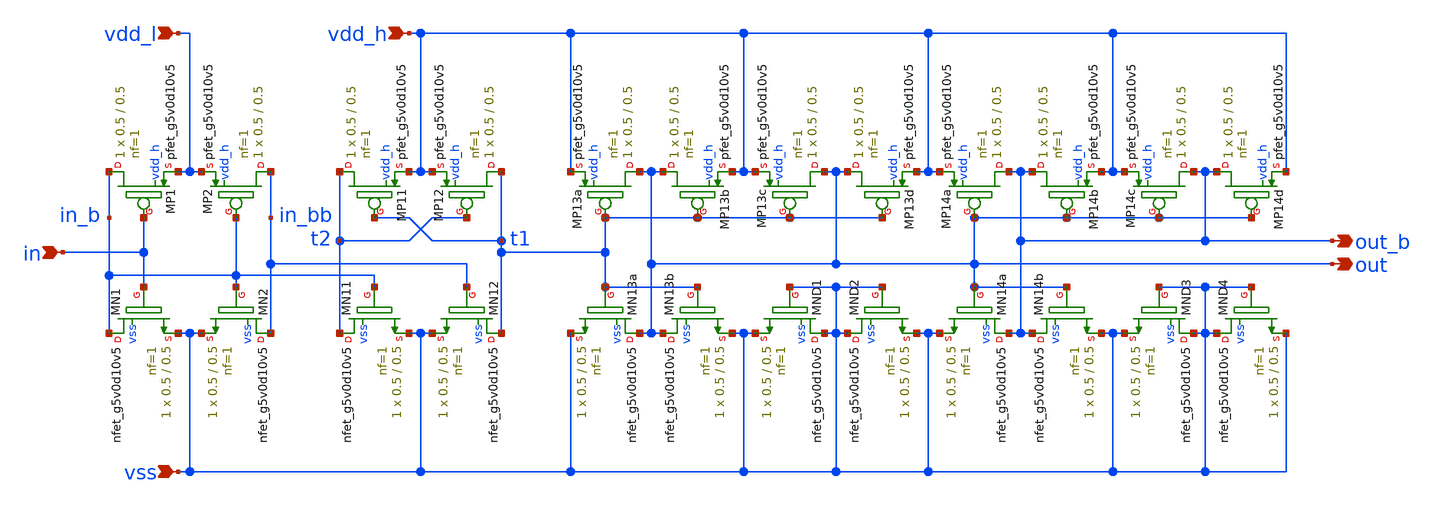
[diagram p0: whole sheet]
** sch_path: xschem/lsi1v8o5v0.sch
**.subckt lsi1v8o5v0 in out_b out vdd_l vdd_h vss
*.ipin in
*.opin out_b
*.opin out
*.ipin vdd_l
*.ipin vdd_h
*.ipin vss
XMN2 in_bb in_b vss vss sky130_fd_pr__nfet_g5v0d10v5 L=0.5 W=0.5 nf=1 ad='int((nf+1)/2) * W/nf * 0.29'
+ as='int((nf+2)/2) * W/nf * 0.29' pd='2*int((nf+1)/2) * (W/nf + 0.29)' ps='2*int((nf+2)/2) * (W/nf + 0.29)'
+ nrd='0.29 / W' nrs='0.29 / W' sa=0 sb=0 sd=0 mult=1 m=1
XMN11 t2 in_b vss vss sky130_fd_pr__nfet_g5v0d10v5 L=0.5 W=0.5 nf=1 ad='int((nf+1)/2) * W/nf * 0.29'
+ as='int((nf+2)/2) * W/nf * 0.29' pd='2*int((nf+1)/2) * (W/nf + 0.29)' ps='2*int((nf+2)/2) * (W/nf + 0.29)'
+ nrd='0.29 / W' nrs='0.29 / W' sa=0 sb=0 sd=0 mult=1 m=1
XMN12 t1 in_bb vss vss sky130_fd_pr__nfet_g5v0d10v5 L=0.5 W=0.5 nf=1 ad='int((nf+1)/2) * W/nf * 0.29'
+ as='int((nf+2)/2) * W/nf * 0.29' pd='2*int((nf+1)/2) * (W/nf + 0.29)' ps='2*int((nf+2)/2) * (W/nf + 0.29)'
+ nrd='0.29 / W' nrs='0.29 / W' sa=0 sb=0 sd=0 mult=1 m=1
XMN13a out t1 vss vss sky130_fd_pr__nfet_g5v0d10v5 L=0.5 W=0.5 nf=1 ad='int((nf+1)/2) * W/nf * 0.29'
+ as='int((nf+2)/2) * W/nf * 0.29' pd='2*int((nf+1)/2) * (W/nf + 0.29)' ps='2*int((nf+2)/2) * (W/nf + 0.29)'
+ nrd='0.29 / W' nrs='0.29 / W' sa=0 sb=0 sd=0 mult=1 m=1
XMN14a out_b out vss vss sky130_fd_pr__nfet_g5v0d10v5 L=0.5 W=0.5 nf=1 ad='int((nf+1)/2) * W/nf * 0.29'
+ as='int((nf+2)/2) * W/nf * 0.29' pd='2*int((nf+1)/2) * (W/nf + 0.29)' ps='2*int((nf+2)/2) * (W/nf + 0.29)'
+ nrd='0.29 / W' nrs='0.29 / W' sa=0 sb=0 sd=0 mult=1 m=1
XMP2 in_bb in_b vdd_l vdd_h sky130_fd_pr__pfet_g5v0d10v5 L=0.5 W=0.5 nf=1 ad='int((nf+1)/2) * W/nf * 0.29'
+ as='int((nf+2)/2) * W/nf * 0.29' pd='2*int((nf+1)/2) * (W/nf + 0.29)' ps='2*int((nf+2)/2) * (W/nf + 0.29)'
+ nrd='0.29 / W' nrs='0.29 / W' sa=0 sb=0 sd=0 mult=1 m=1
XMP11 t2 t1 vdd_h vdd_h sky130_fd_pr__pfet_g5v0d10v5 L=0.5 W=0.5 nf=1 ad='int((nf+1)/2) * W/nf * 0.29'
+ as='int((nf+2)/2) * W/nf * 0.29' pd='2*int((nf+1)/2) * (W/nf + 0.29)' ps='2*int((nf+2)/2) * (W/nf + 0.29)'
+ nrd='0.29 / W' nrs='0.29 / W' sa=0 sb=0 sd=0 mult=1 m=1
XMP12 t1 t2 vdd_h vdd_h sky130_fd_pr__pfet_g5v0d10v5 L=0.5 W=0.5 nf=1 ad='int((nf+1)/2) * W/nf * 0.29'
+ as='int((nf+2)/2) * W/nf * 0.29' pd='2*int((nf+1)/2) * (W/nf + 0.29)' ps='2*int((nf+2)/2) * (W/nf + 0.29)'
+ nrd='0.29 / W' nrs='0.29 / W' sa=0 sb=0 sd=0 mult=1 m=1
XMP13a out t1 vdd_h vdd_h sky130_fd_pr__pfet_g5v0d10v5 L=0.5 W=0.5 nf=1 ad='int((nf+1)/2) * W/nf * 0.29'
+ as='int((nf+2)/2) * W/nf * 0.29' pd='2*int((nf+1)/2) * (W/nf + 0.29)' ps='2*int((nf+2)/2) * (W/nf + 0.29)'
+ nrd='0.29 / W' nrs='0.29 / W' sa=0 sb=0 sd=0 mult=1 m=1
XMP14a out_b out vdd_h vdd_h sky130_fd_pr__pfet_g5v0d10v5 L=0.5 W=0.5 nf=1 ad='int((nf+1)/2) * W/nf * 0.29'
+ as='int((nf+2)/2) * W/nf * 0.29' pd='2*int((nf+1)/2) * (W/nf + 0.29)' ps='2*int((nf+2)/2) * (W/nf + 0.29)'
+ nrd='0.29 / W' nrs='0.29 / W' sa=0 sb=0 sd=0 mult=1 m=1
XMN13b out t1 vss vss sky130_fd_pr__nfet_g5v0d10v5 L=0.5 W=0.5 nf=1 ad='int((nf+1)/2) * W/nf * 0.29'
+ as='int((nf+2)/2) * W/nf * 0.29' pd='2*int((nf+1)/2) * (W/nf + 0.29)' ps='2*int((nf+2)/2) * (W/nf + 0.29)'
+ nrd='0.29 / W' nrs='0.29 / W' sa=0 sb=0 sd=0 mult=1 m=1
XMP13b out t1 vdd_h vdd_h sky130_fd_pr__pfet_g5v0d10v5 L=0.5 W=0.5 nf=1 ad='int((nf+1)/2) * W/nf * 0.29'
+ as='int((nf+2)/2) * W/nf * 0.29' pd='2*int((nf+1)/2) * (W/nf + 0.29)' ps='2*int((nf+2)/2) * (W/nf + 0.29)'
+ nrd='0.29 / W' nrs='0.29 / W' sa=0 sb=0 sd=0 mult=1 m=1
XMP13c out t1 vdd_h vdd_h sky130_fd_pr__pfet_g5v0d10v5 L=0.5 W=0.5 nf=1 ad='int((nf+1)/2) * W/nf * 0.29'
+ as='int((nf+2)/2) * W/nf * 0.29' pd='2*int((nf+1)/2) * (W/nf + 0.29)' ps='2*int((nf+2)/2) * (W/nf + 0.29)'
+ nrd='0.29 / W' nrs='0.29 / W' sa=0 sb=0 sd=0 mult=1 m=1
XMP13d out t1 vdd_h vdd_h sky130_fd_pr__pfet_g5v0d10v5 L=0.5 W=0.5 nf=1 ad='int((nf+1)/2) * W/nf * 0.29'
+ as='int((nf+2)/2) * W/nf * 0.29' pd='2*int((nf+1)/2) * (W/nf + 0.29)' ps='2*int((nf+2)/2) * (W/nf + 0.29)'
+ nrd='0.29 / W' nrs='0.29 / W' sa=0 sb=0 sd=0 mult=1 m=1
XMND1 vss vss vss vss sky130_fd_pr__nfet_g5v0d10v5 L=0.5 W=0.5 nf=1 ad='int((nf+1)/2) * W/nf * 0.29'
+ as='int((nf+2)/2) * W/nf * 0.29' pd='2*int((nf+1)/2) * (W/nf + 0.29)' ps='2*int((nf+2)/2) * (W/nf + 0.29)'
+ nrd='0.29 / W' nrs='0.29 / W' sa=0 sb=0 sd=0 mult=1 m=1
XMND2 vss vss vss vss sky130_fd_pr__nfet_g5v0d10v5 L=0.5 W=0.5 nf=1 ad='int((nf+1)/2) * W/nf * 0.29'
+ as='int((nf+2)/2) * W/nf * 0.29' pd='2*int((nf+1)/2) * (W/nf + 0.29)' ps='2*int((nf+2)/2) * (W/nf + 0.29)'
+ nrd='0.29 / W' nrs='0.29 / W' sa=0 sb=0 sd=0 mult=1 m=1
XMP14b out_b out vdd_h vdd_h sky130_fd_pr__pfet_g5v0d10v5 L=0.5 W=0.5 nf=1 ad='int((nf+1)/2) * W/nf * 0.29'
+ as='int((nf+2)/2) * W/nf * 0.29' pd='2*int((nf+1)/2) * (W/nf + 0.29)' ps='2*int((nf+2)/2) * (W/nf + 0.29)'
+ nrd='0.29 / W' nrs='0.29 / W' sa=0 sb=0 sd=0 mult=1 m=1
XMP14c out_b out vdd_h vdd_h sky130_fd_pr__pfet_g5v0d10v5 L=0.5 W=0.5 nf=1 ad='int((nf+1)/2) * W/nf * 0.29'
+ as='int((nf+2)/2) * W/nf * 0.29' pd='2*int((nf+1)/2) * (W/nf + 0.29)' ps='2*int((nf+2)/2) * (W/nf + 0.29)'
+ nrd='0.29 / W' nrs='0.29 / W' sa=0 sb=0 sd=0 mult=1 m=1
XMP14d out_b out vdd_h vdd_h sky130_fd_pr__pfet_g5v0d10v5 L=0.5 W=0.5 nf=1 ad='int((nf+1)/2) * W/nf * 0.29'
+ as='int((nf+2)/2) * W/nf * 0.29' pd='2*int((nf+1)/2) * (W/nf + 0.29)' ps='2*int((nf+2)/2) * (W/nf + 0.29)'
+ nrd='0.29 / W' nrs='0.29 / W' sa=0 sb=0 sd=0 mult=1 m=1
XMN14b out_b out vss vss sky130_fd_pr__nfet_g5v0d10v5 L=0.5 W=0.5 nf=1 ad='int((nf+1)/2) * W/nf * 0.29'
+ as='int((nf+2)/2) * W/nf * 0.29' pd='2*int((nf+1)/2) * (W/nf + 0.29)' ps='2*int((nf+2)/2) * (W/nf + 0.29)'
+ nrd='0.29 / W' nrs='0.29 / W' sa=0 sb=0 sd=0 mult=1 m=1
XMND3 vss vss vss vss sky130_fd_pr__nfet_g5v0d10v5 L=0.5 W=0.5 nf=1 ad='int((nf+1)/2) * W/nf * 0.29'
+ as='int((nf+2)/2) * W/nf * 0.29' pd='2*int((nf+1)/2) * (W/nf + 0.29)' ps='2*int((nf+2)/2) * (W/nf + 0.29)'
+ nrd='0.29 / W' nrs='0.29 / W' sa=0 sb=0 sd=0 mult=1 m=1
XMND4 vss vss vss vss sky130_fd_pr__nfet_g5v0d10v5 L=0.5 W=0.5 nf=1 ad='int((nf+1)/2) * W/nf * 0.29'
+ as='int((nf+2)/2) * W/nf * 0.29' pd='2*int((nf+1)/2) * (W/nf + 0.29)' ps='2*int((nf+2)/2) * (W/nf + 0.29)'
+ nrd='0.29 / W' nrs='0.29 / W' sa=0 sb=0 sd=0 mult=1 m=1
XMP1 in_b in vdd_l vdd_h sky130_fd_pr__pfet_g5v0d10v5 L=0.5 W=0.5 nf=1 ad='int((nf+1)/2) * W/nf * 0.29'
+ as='int((nf+2)/2) * W/nf * 0.29' pd='2*int((nf+1)/2) * (W/nf + 0.29)' ps='2*int((nf+2)/2) * (W/nf + 0.29)'
+ nrd='0.29 / W' nrs='0.29 / W' sa=0 sb=0 sd=0 mult=1 m=1
XMN1 in_b in vss vss sky130_fd_pr__nfet_g5v0d10v5 L=0.5 W=0.5 nf=1 ad='int((nf+1)/2) * W/nf * 0.29' as='int((nf+2)/2) * W/nf * 0.29'
+ pd='2*int((nf+1)/2) * (W/nf + 0.29)' ps='2*int((nf+2)/2) * (W/nf + 0.29)' nrd='0.29 / W' nrs='0.29 / W'
+ sa=0 sb=0 sd=0 mult=1 m=1
**.ends
.end
